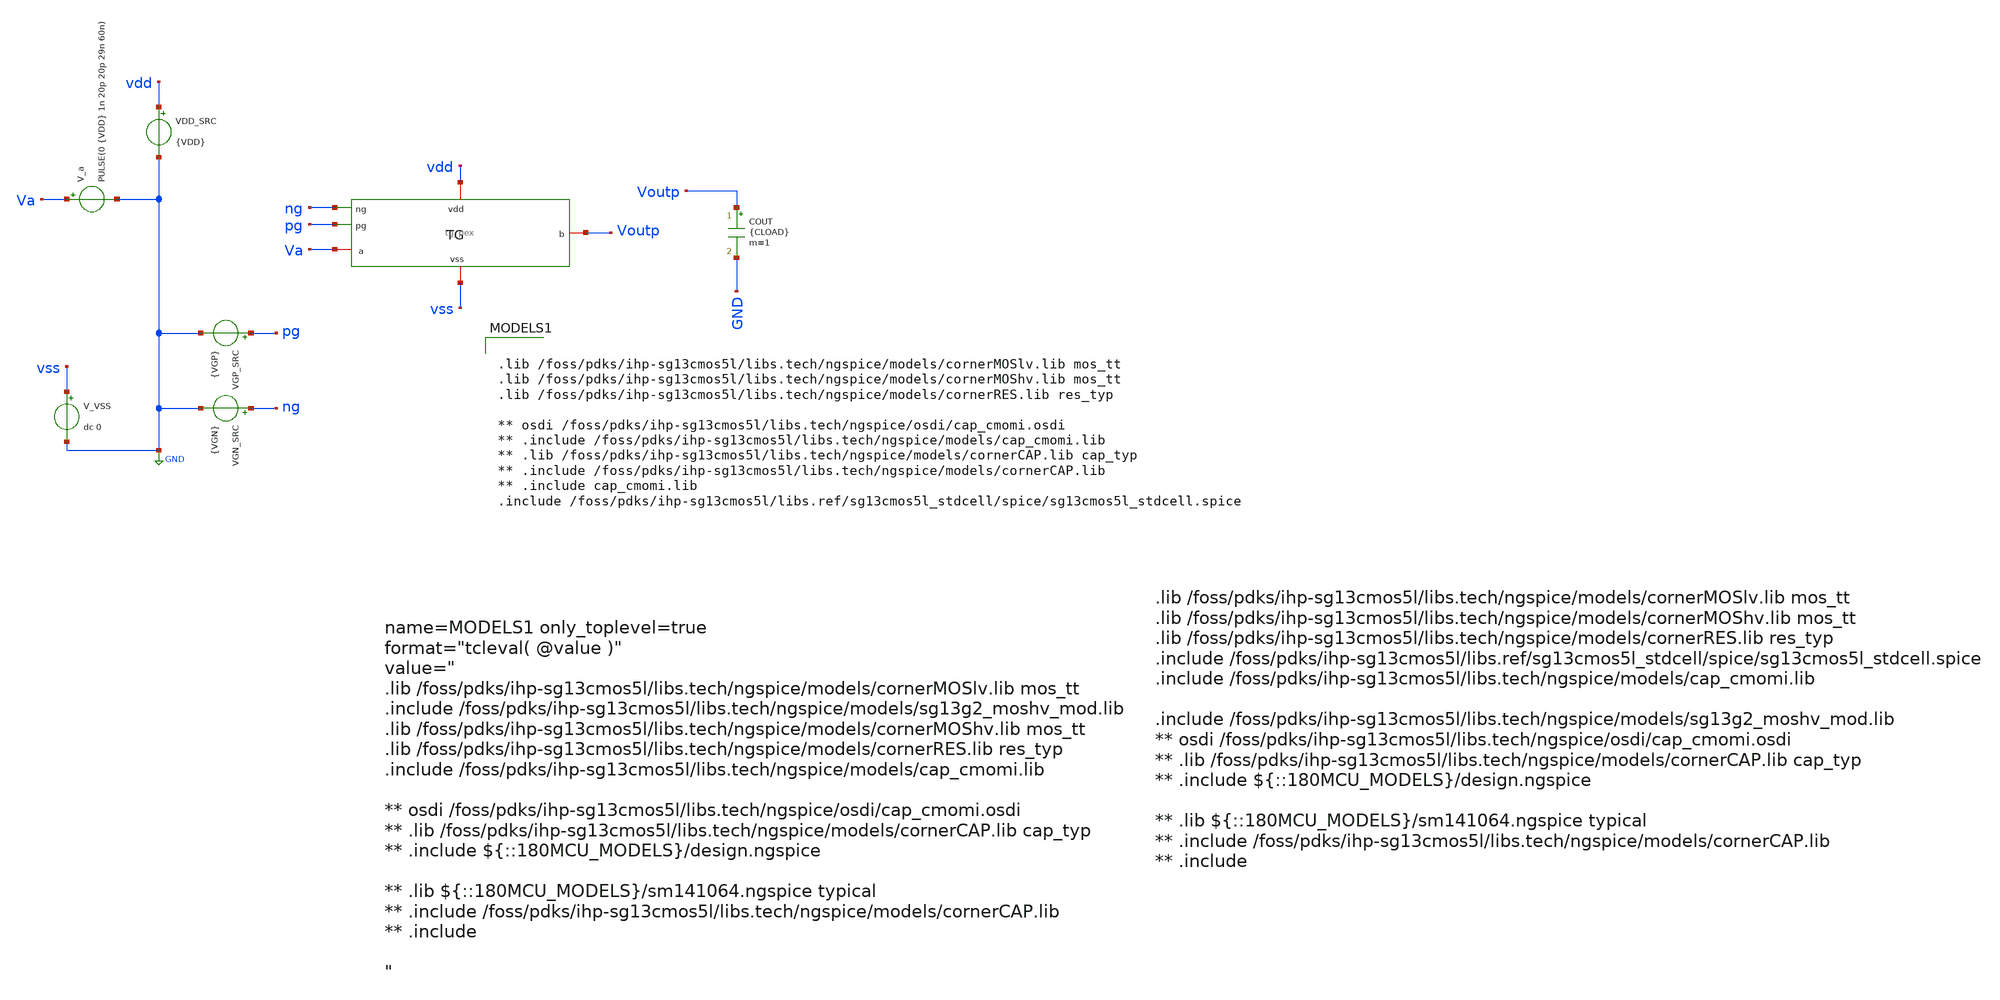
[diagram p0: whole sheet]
** sch_path: circuit_files/tb/tg_tb_pex.sch
**.subckt tg_tb_pex
VGN_SRC ng GND {VGN}
VDD_SRC vdd GND {VDD}
VGP_SRC pg GND {VGP}
V_a Va GND PULSE(0 {VDD} 1n 20p 20p 29n 60n)
V_VSS vss GND dc 0
COUT Voutp GND {CLOAD} m=1
x2 vss ng pg vdd Va Voutp tg_pex
**** begin user architecture code


.include /foss/designs/SAR_ADC_IHP/circuit_files/layout/tg/pex/tg.pex.spice

.param VDD=3.3
.param VGN=3.3
.param VGP=0
.param CLOAD=5.12p

.save v(Va) v(Voutp) v(ng) v(pg) i(VDD_SRC)

.control
tran 2p 120n
write tg_pex_transient.raw v(Va) v(Voutp) v(ng) v(pg) i(VDD_SRC)

meas tran Va_9ns FIND v(Va) AT=9n
meas tran Vout_9ns FIND v(Voutp) AT=9n
meas tran Va_16ns FIND v(Va) AT=16n
meas tran Vout_16ns FIND v(Voutp) AT=16n

plot v(Va) v(Voutp) v(ng) v(pg)
.endc




.lib /foss/pdks/ihp-sg13cmos5l/libs.tech/ngspice/models/cornerMOSlv.lib mos_tt
.lib /foss/pdks/ihp-sg13cmos5l/libs.tech/ngspice/models/cornerMOShv.lib mos_tt
.lib /foss/pdks/ihp-sg13cmos5l/libs.tech/ngspice/models/cornerRES.lib res_typ

** osdi /foss/pdks/ihp-sg13cmos5l/libs.tech/ngspice/osdi/cap_cmomi.osdi
** .include /foss/pdks/ihp-sg13cmos5l/libs.tech/ngspice/models/cap_cmomi.lib
** .lib /foss/pdks/ihp-sg13cmos5l/libs.tech/ngspice/models/cornerCAP.lib cap_typ
** .include /foss/pdks/ihp-sg13cmos5l/libs.tech/ngspice/models/cornerCAP.lib
** .include cap_cmomi.lib
.include /foss/pdks/ihp-sg13cmos5l/libs.ref/sg13cmos5l_stdcell/spice/sg13cmos5l_stdcell.spice

**** end user architecture code
**.ends
.GLOBAL GND
.end
